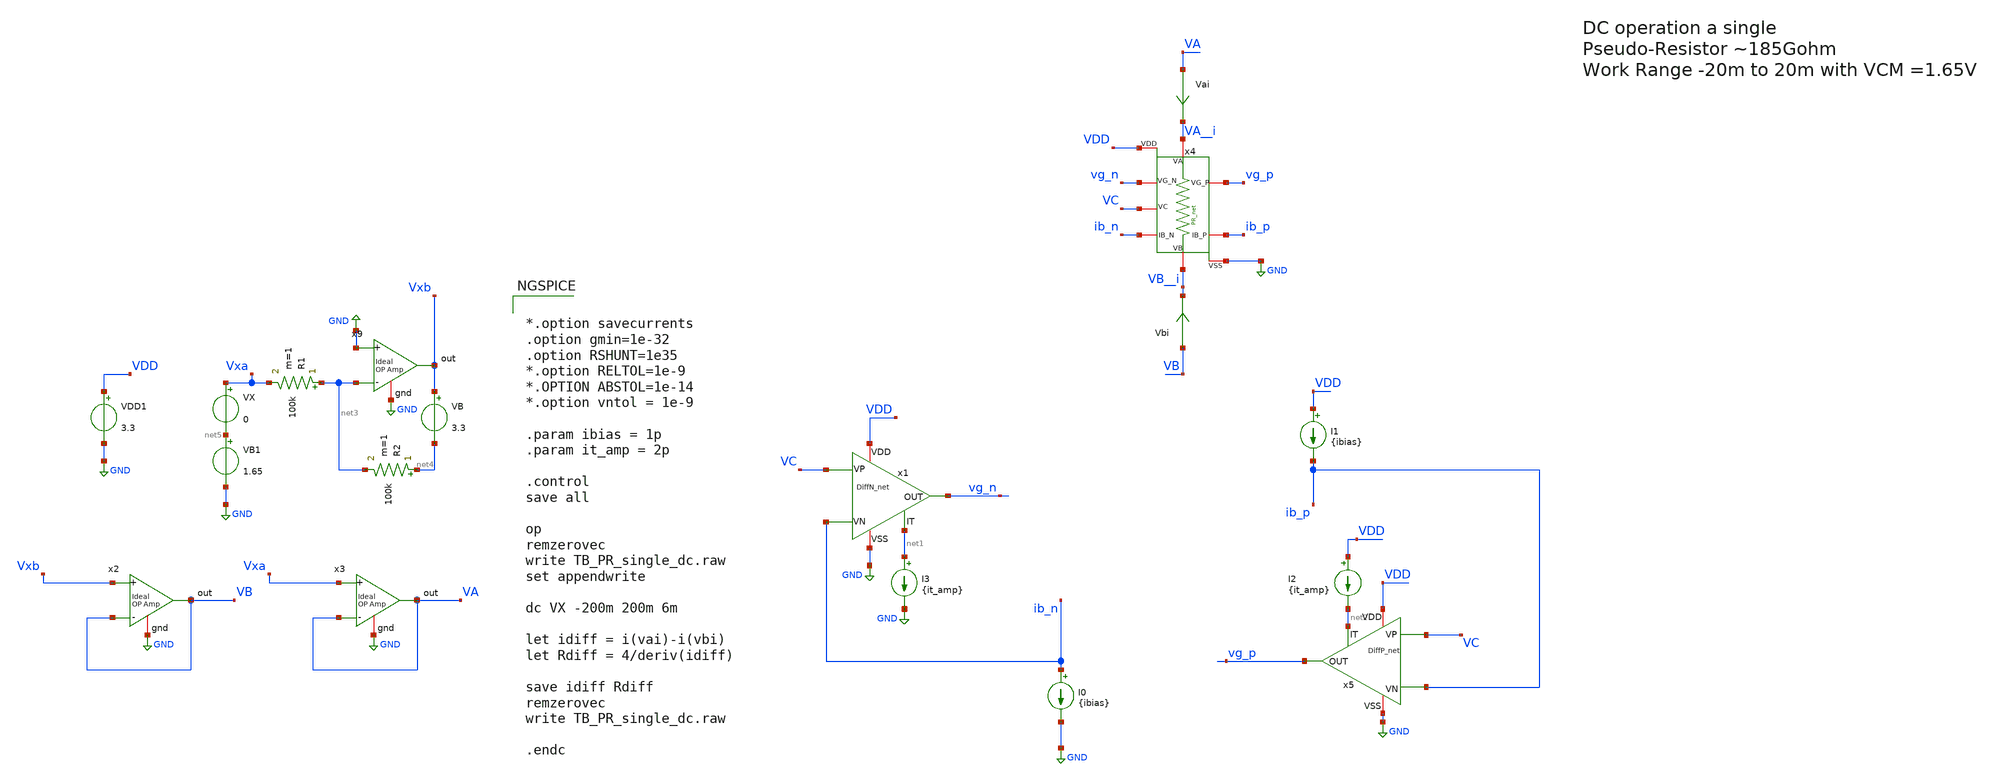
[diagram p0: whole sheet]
** sch_path: TIA/PseudoResistor/TB_PR_single_dc.sch
**.subckt TB_PR_single_dc
I0 ib_n GND {ibias}
I1 VDD ib_p {ibias}
VDD1 VDD GND 3.3
I2 VDD net2 {it_amp}
I3 net1 GND {it_amp}
VX Vxa net5 0
VB Vxb net4 3.3
R1 net3 Vxa 100k m=1
R2 net4 net3 100k m=1
VB1 net5 GND 1.65
x2 VB Vxb VB GND ampOp_ideal
x3 VA Vxa VA GND ampOp_ideal
x9 Vxb GND net3 GND ampOp_ideal
Vbi VB VB__i 0
.save i(vbi)
Vai VA VA__i 0
.save i(vai)
x4 VA__i VB__i vg_n vg_p ib_n ib_p VC VDD GND PR_net
x1 ib_n VC vg_n net1 VDD GND DiffN_net
x5 ib_p VC vg_p net2 VDD GND DiffP_net
**** begin user architecture code

.include $::180MCU_MODELS/design.ngspice
.lib $::180MCU_MODELS/sm141064.ngspice typical

*.include /home/gmaranhao/Desktop/gf180_work/TIA/PseudoResistor/layout/spice/PR_net_pex.spice

*.include /home/gmaranhao/Desktop/gf180_work/TIA/PseudoResistor/layout/spice/PR_pfets_pex.spice
*.include /home/gmaranhao/Desktop/gf180_work/TIA/PseudoResistor/layout/spice/PR_nfets_pex.spice

*.subckt PR_net VSS VC VG_N IB_N VDD VB VA IB_P VG_P
*X1 0 VC vg_n ib_n VDD VB__i VA__i ib_p vg_p PR_net

*.subckt PR_nfets VD2 VG VC VS2 VS1 VD1 VB
*X2 VC_A vg_n VC VC_B ib_n VDD 0 PR_nfets

*   PR_pfets VS2_A VG VS2_B VC_A VC_B VS1 VD1 VB
*X3 VA__i vg_p VB__i VC_A VC_B 0 ib_p VDD PR_pfets





*.option savecurrents
.option gmin=1e-32
.option RSHUNT=1e35
*.option RELTOL=1e-9
*.OPTION ABSTOL=1e-14
*.option vntol = 1e-9

.param ibias = 1p
.param it_amp = 2p

.control
save all

op
remzerovec
write TB_PR_single_dc.raw
set appendwrite

dc VX -200m 200m 6m

let idiff = i(vai)-i(vbi)
let Rdiff = 4/deriv(idiff)

save idiff Rdiff
remzerovec
write TB_PR_single_dc.raw

.endc


**** end user architecture code
**.ends
.GLOBAL GND
.end
